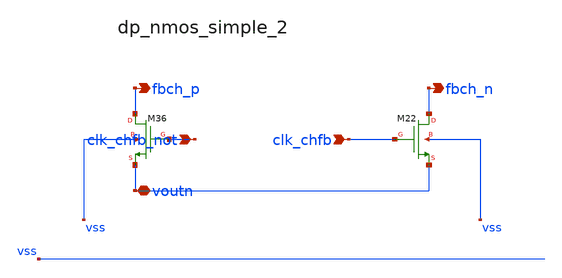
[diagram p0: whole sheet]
** sch_path: analog-db/raw/ia_002_fan_chopper_simple/hier/blocks/dp_nmos_simple_2.sch
**.subckt dp_nmos_simple_2 clk_chfb_not clk_chfb voutn fbch_p fbch_n
*.ipin clk_chfb_not
*.ipin clk_chfb
*.iopin voutn
*.opin fbch_p
*.opin fbch_n
XM22 fbch_n clk_chfb voutn vss sg13_lv_nmos w=x_dut_xm22_w l=x_dut_xm22_l ng=1 m=x_dut_xm22_m
XM36 fbch_p clk_chfb_not voutn vss sg13_lv_nmos w=x_dut_xm36_w l=x_dut_xm36_l ng=1 m=x_dut_xm36_m
**.ends
.end
